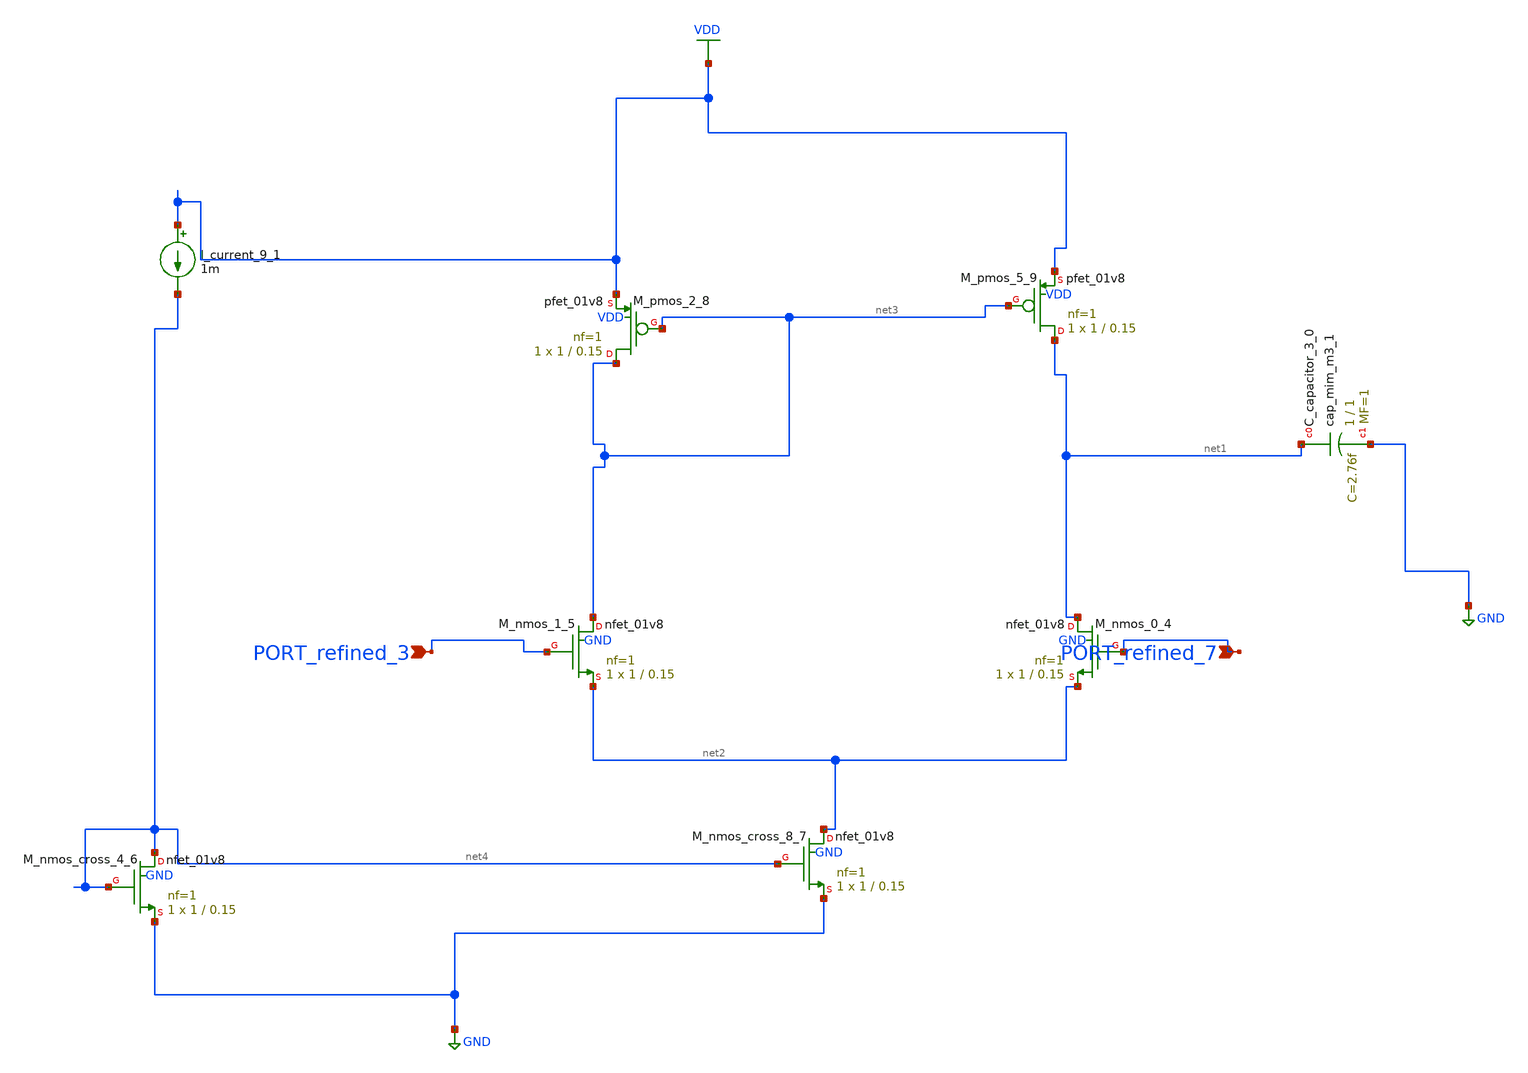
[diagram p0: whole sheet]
** sch_path: schematics/Image2Net/117.sch
**.subckt 117 PORT_refined_3 PORT_refined_7
*.ipin PORT_refined_3
*.ipin PORT_refined_7
XC_capacitor_3_0 net1 GND sky130_fd_pr__cap_mim_m3_1 W=1 L=1 MF=1 m=1
I_current_9_1 VDD net4 1m
XM_nmos_0_4 net1 PORT_refined_7 net2 GND sky130_fd_pr__nfet_01v8 L=0.15 W=1 nf=1 ad='int((1 + 1)/2) * 1 / 1 * 0.29'
+ as='int((1 + 2)/2) * 1 / 1 * 0.29' pd='2*int((1 + 1)/2) * (1 / 1 + 0.29)' ps='2*int((1 + 2)/2) * (1 / 1 + 0.29)'
+ nrd='0.29 / 1 ' nrs='0.29 / 1 ' sa=0 sb=0 sd=0 mult=1 m=1
XM_nmos_1_5 net3 PORT_refined_3 net2 GND sky130_fd_pr__nfet_01v8 L=0.15 W=1 nf=1 ad='int((1 + 1)/2) * 1 / 1 * 0.29'
+ as='int((1 + 2)/2) * 1 / 1 * 0.29' pd='2*int((1 + 1)/2) * (1 / 1 + 0.29)' ps='2*int((1 + 2)/2) * (1 / 1 + 0.29)'
+ nrd='0.29 / 1 ' nrs='0.29 / 1 ' sa=0 sb=0 sd=0 mult=1 m=1
XM_nmos_cross_4_6 net4 net4 GND GND sky130_fd_pr__nfet_01v8 L=0.15 W=1 nf=1 ad='int((1 + 1)/2) * 1 / 1 * 0.29'
+ as='int((1 + 2)/2) * 1 / 1 * 0.29' pd='2*int((1 + 1)/2) * (1 / 1 + 0.29)' ps='2*int((1 + 2)/2) * (1 / 1 + 0.29)'
+ nrd='0.29 / 1 ' nrs='0.29 / 1 ' sa=0 sb=0 sd=0 mult=1 m=1
XM_nmos_cross_8_7 net2 net4 GND GND sky130_fd_pr__nfet_01v8 L=0.15 W=1 nf=1 ad='int((1 + 1)/2) * 1 / 1 * 0.29'
+ as='int((1 + 2)/2) * 1 / 1 * 0.29' pd='2*int((1 + 1)/2) * (1 / 1 + 0.29)' ps='2*int((1 + 2)/2) * (1 / 1 + 0.29)'
+ nrd='0.29 / 1 ' nrs='0.29 / 1 ' sa=0 sb=0 sd=0 mult=1 m=1
XM_pmos_2_8 net3 net3 VDD VDD sky130_fd_pr__pfet_01v8 L=0.15 W=1 nf=1 ad='int((1 + 1)/2) * 1 / 1 * 0.29'
+ as='int((1 + 2)/2) * 1 / 1 * 0.29' pd='2*int((1 + 1)/2) * (1 / 1 + 0.29)' ps='2*int((1 + 2)/2) * (1 / 1 + 0.29)'
+ nrd='0.29 / 1 ' nrs='0.29 / 1 ' sa=0 sb=0 sd=0 mult=1 m=1
XM_pmos_5_9 net1 net3 VDD VDD sky130_fd_pr__pfet_01v8 L=0.15 W=1 nf=1 ad='int((1 + 1)/2) * 1 / 1 * 0.29'
+ as='int((1 + 2)/2) * 1 / 1 * 0.29' pd='2*int((1 + 1)/2) * (1 / 1 + 0.29)' ps='2*int((1 + 2)/2) * (1 / 1 + 0.29)'
+ nrd='0.29 / 1 ' nrs='0.29 / 1 ' sa=0 sb=0 sd=0 mult=1 m=1
**.ends
.GLOBAL GND
.GLOBAL VDD
.end
